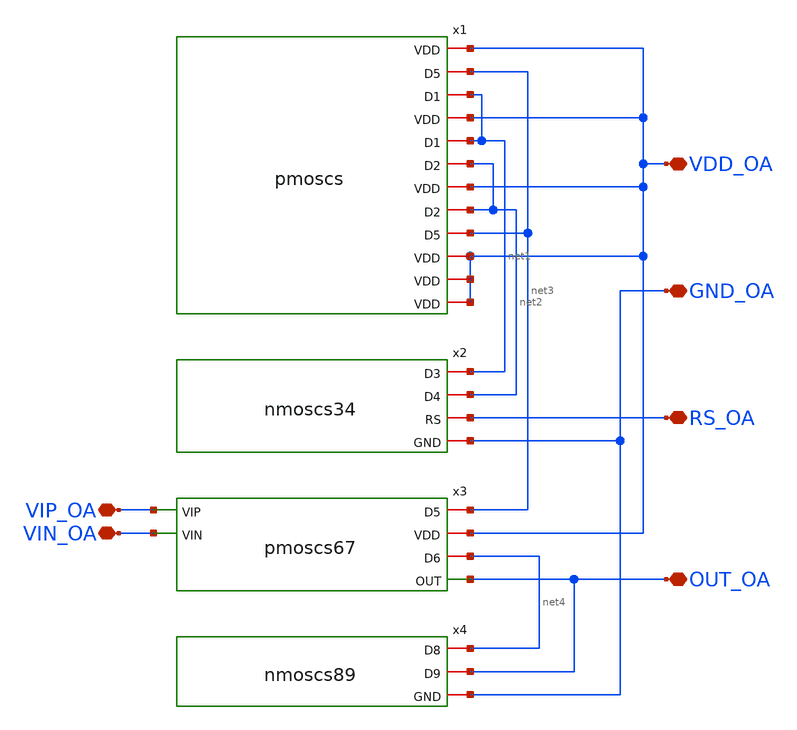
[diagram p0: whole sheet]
** sch_path: opamp/mag/opamp.sch
**.subckt opamp VDD_OA GND_OA RS_OA OUT_OA VIP_OA VIN_OA
*.iopin VDD_OA
*.iopin GND_OA
*.iopin RS_OA
*.iopin OUT_OA
*.iopin VIP_OA
*.iopin VIN_OA
x1 VDD_OA net3 net1 net2 pmoscs
x2 net1 net2 RS_OA GND_OA nmoscs34
x3 net3 VDD_OA VIP_OA VIN_OA net4 OUT_OA pmoscs67
x4 net4 OUT_OA GND_OA nmoscs89
**.ends
.end
